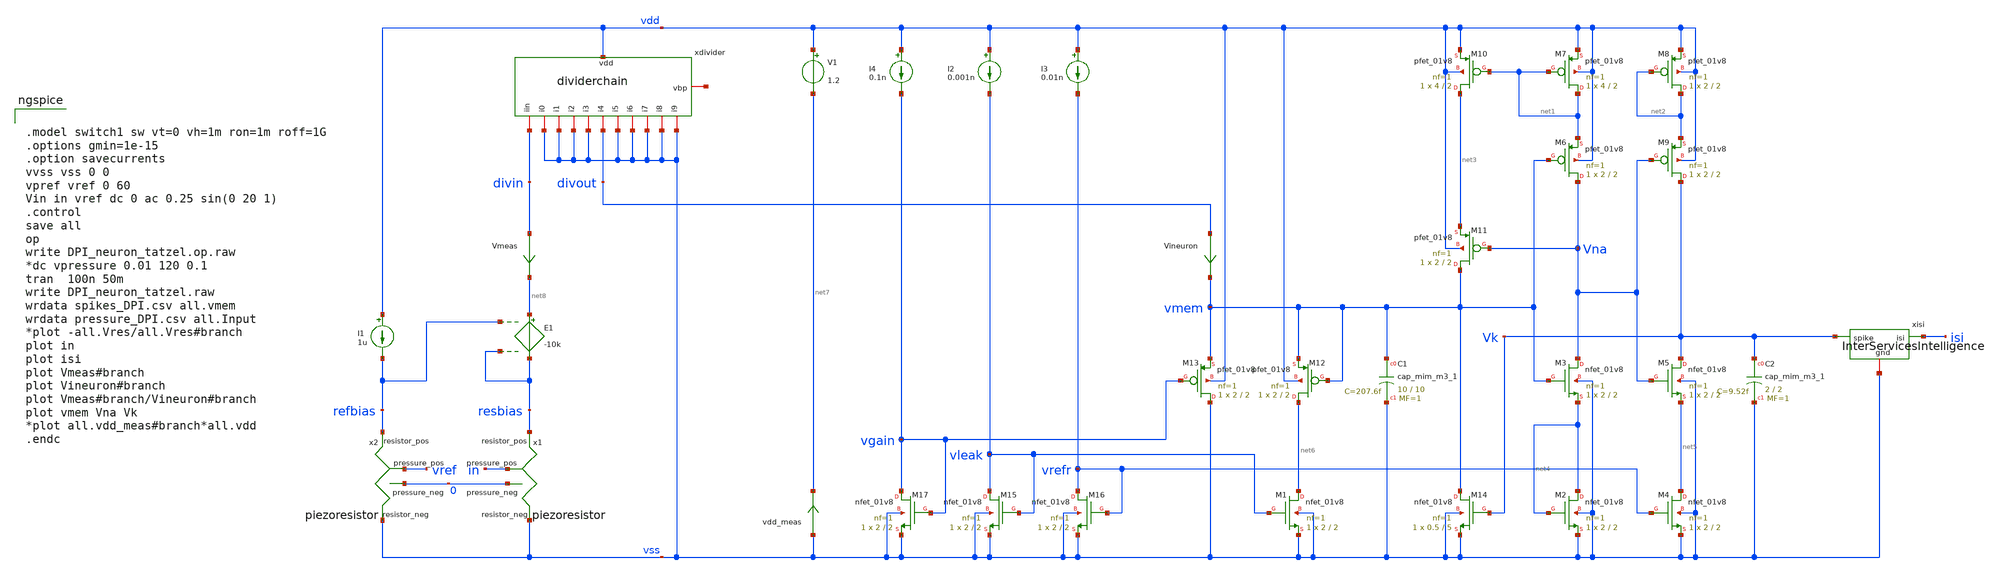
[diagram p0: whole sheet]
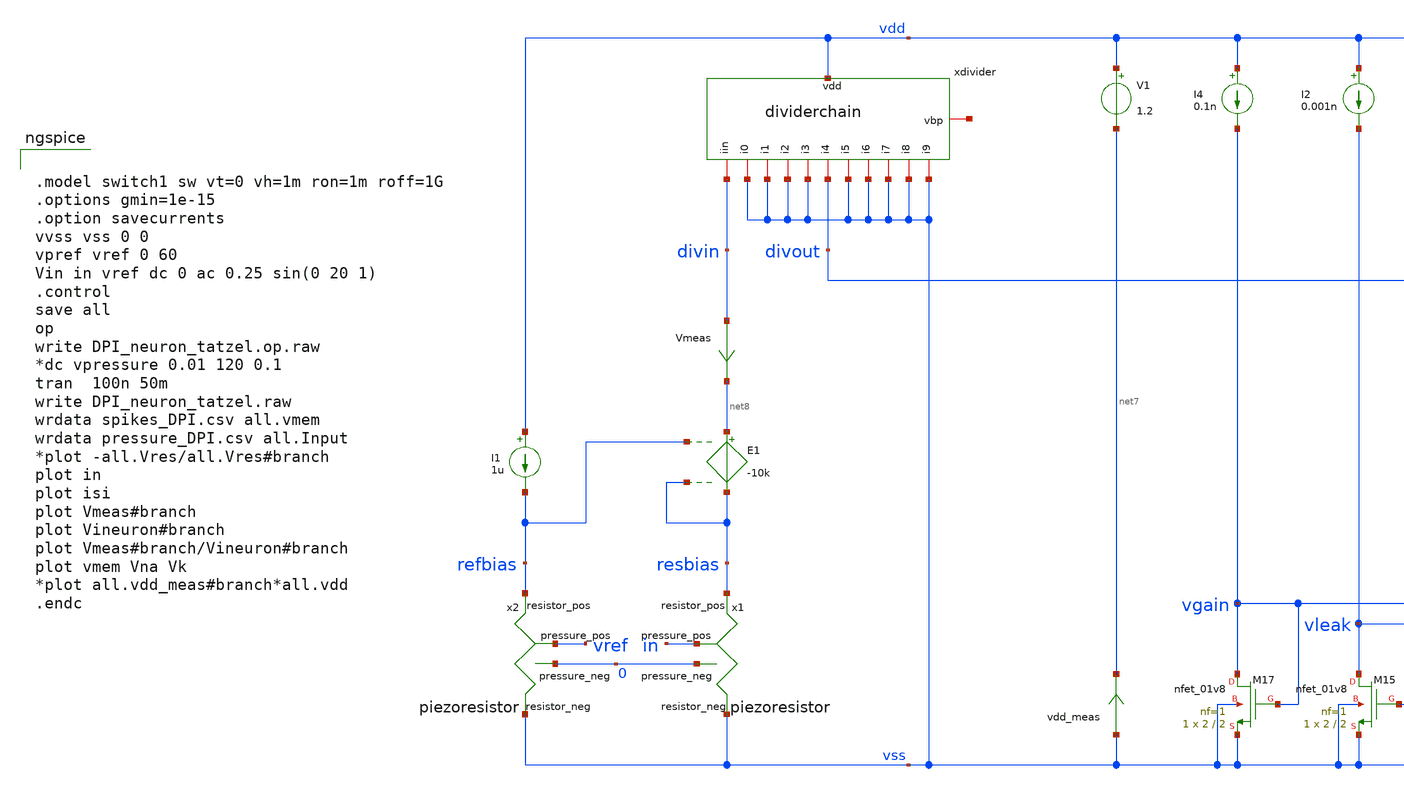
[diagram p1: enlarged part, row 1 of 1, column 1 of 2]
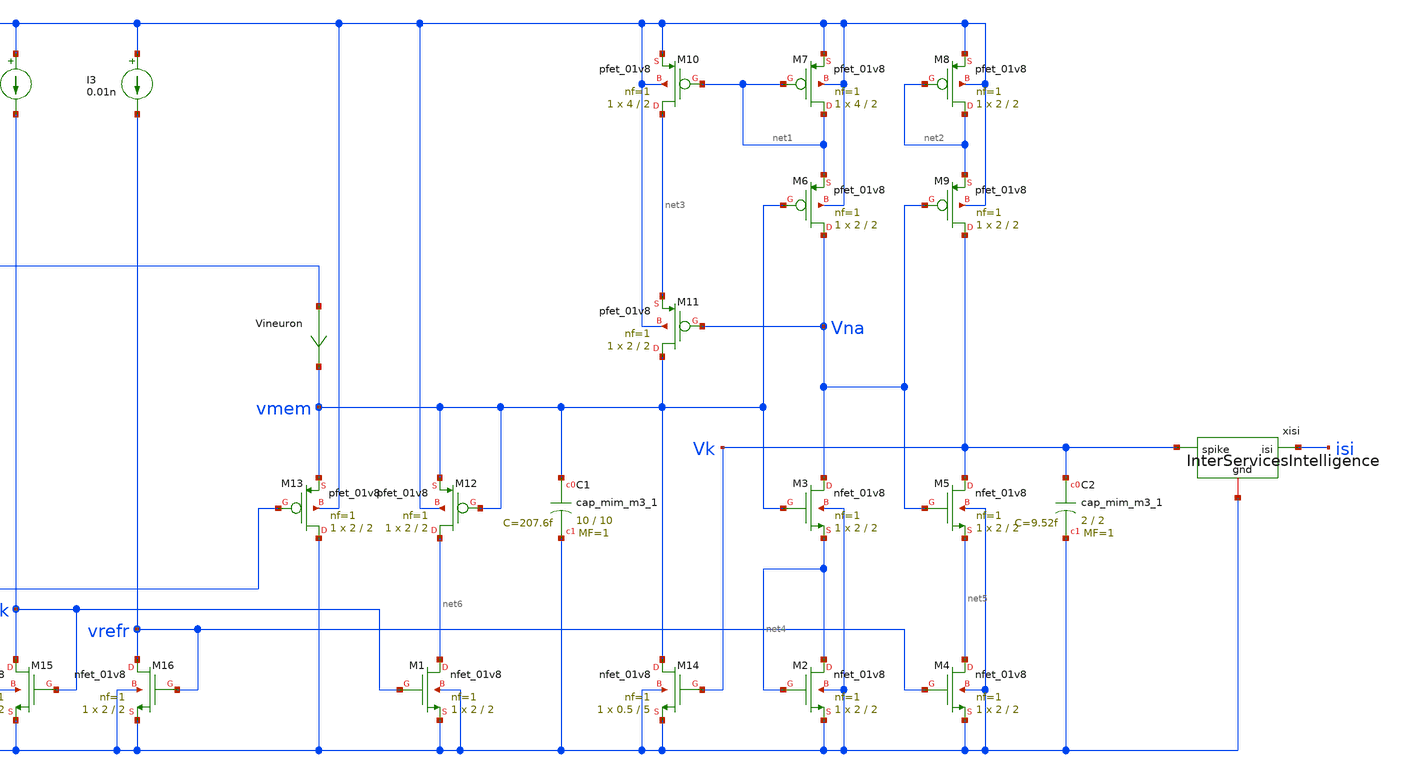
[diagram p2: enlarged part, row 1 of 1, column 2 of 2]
** sch_path: circuits/DPI_neuron_tatzel.sch
* piezoresistor.sch:
* Copyright 2020 Stefan Frederik Schippers
* Licensed under the Apache License, Version 2.0 (the "License");
**.subckt DPI_neuron_tatzel
Vmeas divin net8 0
.save i(vmeas)
vdd_meas vss net7 0
.save i(vdd_meas)
V1 vdd net7 1.2
XM1 net6 vleak vss vss sky130_fd_pr__nfet_01v8 L=2 W=2 nf=1 ad='int((nf+1)/2) * W/nf * 0.29' as='int((nf+2)/2) * W/nf * 0.29'
+ pd='2*int((nf+1)/2) * (W/nf + 0.29)' ps='2*int((nf+2)/2) * (W/nf + 0.29)' nrd='0.29 / W' nrs='0.29 / W'
+ sa=0 sb=0 sd=0 mult=1 m=1
XM2 net4 net4 vss vss sky130_fd_pr__nfet_01v8 L=2 W=2 nf=1 ad='int((nf+1)/2) * W/nf * 0.29' as='int((nf+2)/2) * W/nf * 0.29'
+ pd='2*int((nf+1)/2) * (W/nf + 0.29)' ps='2*int((nf+2)/2) * (W/nf + 0.29)' nrd='0.29 / W' nrs='0.29 / W'
+ sa=0 sb=0 sd=0 mult=1 m=1
XM3 Vna vmem net4 vss sky130_fd_pr__nfet_01v8 L=2 W=2 nf=1 ad='int((nf+1)/2) * W/nf * 0.29' as='int((nf+2)/2) * W/nf * 0.29'
+ pd='2*int((nf+1)/2) * (W/nf + 0.29)' ps='2*int((nf+2)/2) * (W/nf + 0.29)' nrd='0.29 / W' nrs='0.29 / W'
+ sa=0 sb=0 sd=0 mult=1 m=1
XC1 vmem vss sky130_fd_pr__cap_mim_m3_1 W=10 L=10 MF=1 m=1
XC2 Vk vss sky130_fd_pr__cap_mim_m3_1 W=2 L=2 MF=1 m=1
XM14 vmem Vk vss vss sky130_fd_pr__nfet_01v8 L=5 W=0.5 nf=1 ad='int((nf+1)/2) * W/nf * 0.29' as='int((nf+2)/2) * W/nf * 0.29'
+ pd='2*int((nf+1)/2) * (W/nf + 0.29)' ps='2*int((nf+2)/2) * (W/nf + 0.29)' nrd='0.29 / W' nrs='0.29 / W'
+ sa=0 sb=0 sd=0 mult=1 m=1
XM4 net5 vrefr vss vss sky130_fd_pr__nfet_01v8 L=2 W=2 nf=1 ad='int((nf+1)/2) * W/nf * 0.29' as='int((nf+2)/2) * W/nf * 0.29'
+ pd='2*int((nf+1)/2) * (W/nf + 0.29)' ps='2*int((nf+2)/2) * (W/nf + 0.29)' nrd='0.29 / W' nrs='0.29 / W'
+ sa=0 sb=0 sd=0 mult=1 m=1
XM5 Vk Vna net5 vss sky130_fd_pr__nfet_01v8 L=2 W=2 nf=1 ad='int((nf+1)/2) * W/nf * 0.29' as='int((nf+2)/2) * W/nf * 0.29'
+ pd='2*int((nf+1)/2) * (W/nf + 0.29)' ps='2*int((nf+2)/2) * (W/nf + 0.29)' nrd='0.29 / W' nrs='0.29 / W'
+ sa=0 sb=0 sd=0 mult=1 m=1
I2 vdd vleak 0.001n
XM15 vleak vleak vss vss sky130_fd_pr__nfet_01v8 L=2 W=2 nf=1 ad='int((nf+1)/2) * W/nf * 0.29' as='int((nf+2)/2) * W/nf * 0.29'
+ pd='2*int((nf+1)/2) * (W/nf + 0.29)' ps='2*int((nf+2)/2) * (W/nf + 0.29)' nrd='0.29 / W' nrs='0.29 / W'
+ sa=0 sb=0 sd=0 mult=1 m=1
I3 vdd vrefr 0.01n
XM16 vrefr vrefr vss vss sky130_fd_pr__nfet_01v8 L=2 W=2 nf=1 ad='int((nf+1)/2) * W/nf * 0.29' as='int((nf+2)/2) * W/nf * 0.29'
+ pd='2*int((nf+1)/2) * (W/nf + 0.29)' ps='2*int((nf+2)/2) * (W/nf + 0.29)' nrd='0.29 / W' nrs='0.29 / W'
+ sa=0 sb=0 sd=0 mult=1 m=1
I4 vdd vgain 0.1n
XM17 vgain vgain vss vss sky130_fd_pr__nfet_01v8 L=2 W=2 nf=1 ad='int((nf+1)/2) * W/nf * 0.29' as='int((nf+2)/2) * W/nf * 0.29'
+ pd='2*int((nf+1)/2) * (W/nf + 0.29)' ps='2*int((nf+2)/2) * (W/nf + 0.29)' nrd='0.29 / W' nrs='0.29 / W'
+ sa=0 sb=0 sd=0 mult=1 m=1
XM6 Vna vmem net1 vdd sky130_fd_pr__pfet_01v8 L=2 W=2 nf=1 ad='int((nf+1)/2) * W/nf * 0.29' as='int((nf+2)/2) * W/nf * 0.29'
+ pd='2*int((nf+1)/2) * (W/nf + 0.29)' ps='2*int((nf+2)/2) * (W/nf + 0.29)' nrd='0.29 / W' nrs='0.29 / W'
+ sa=0 sb=0 sd=0 mult=1 m=1
XM7 net1 net1 vdd vdd sky130_fd_pr__pfet_01v8 L=2 W=4 nf=1 ad='int((nf+1)/2) * W/nf * 0.29' as='int((nf+2)/2) * W/nf * 0.29'
+ pd='2*int((nf+1)/2) * (W/nf + 0.29)' ps='2*int((nf+2)/2) * (W/nf + 0.29)' nrd='0.29 / W' nrs='0.29 / W'
+ sa=0 sb=0 sd=0 mult=1 m=1
XM8 net2 net2 vdd vdd sky130_fd_pr__pfet_01v8 L=2 W=2 nf=1 ad='int((nf+1)/2) * W/nf * 0.29' as='int((nf+2)/2) * W/nf * 0.29'
+ pd='2*int((nf+1)/2) * (W/nf + 0.29)' ps='2*int((nf+2)/2) * (W/nf + 0.29)' nrd='0.29 / W' nrs='0.29 / W'
+ sa=0 sb=0 sd=0 mult=1 m=1
XM9 Vk Vna net2 vdd sky130_fd_pr__pfet_01v8 L=2 W=2 nf=1 ad='int((nf+1)/2) * W/nf * 0.29' as='int((nf+2)/2) * W/nf * 0.29'
+ pd='2*int((nf+1)/2) * (W/nf + 0.29)' ps='2*int((nf+2)/2) * (W/nf + 0.29)' nrd='0.29 / W' nrs='0.29 / W'
+ sa=0 sb=0 sd=0 mult=1 m=1
XM10 net3 net1 vdd vdd sky130_fd_pr__pfet_01v8 L=2 W=4 nf=1 ad='int((nf+1)/2) * W/nf * 0.29' as='int((nf+2)/2) * W/nf * 0.29'
+ pd='2*int((nf+1)/2) * (W/nf + 0.29)' ps='2*int((nf+2)/2) * (W/nf + 0.29)' nrd='0.29 / W' nrs='0.29 / W'
+ sa=0 sb=0 sd=0 mult=1 m=1
XM11 vmem Vna net3 vdd sky130_fd_pr__pfet_01v8 L=2 W=2 nf=1 ad='int((nf+1)/2) * W/nf * 0.29' as='int((nf+2)/2) * W/nf * 0.29'
+ pd='2*int((nf+1)/2) * (W/nf + 0.29)' ps='2*int((nf+2)/2) * (W/nf + 0.29)' nrd='0.29 / W' nrs='0.29 / W'
+ sa=0 sb=0 sd=0 mult=1 m=1
XM12 net6 vmem vmem vdd sky130_fd_pr__pfet_01v8 L=2 W=2 nf=1 ad='int((nf+1)/2) * W/nf * 0.29' as='int((nf+2)/2) * W/nf * 0.29'
+ pd='2*int((nf+1)/2) * (W/nf + 0.29)' ps='2*int((nf+2)/2) * (W/nf + 0.29)' nrd='0.29 / W' nrs='0.29 / W'
+ sa=0 sb=0 sd=0 mult=1 m=1
XM13 vss vgain vmem vdd sky130_fd_pr__pfet_01v8 L=2 W=2 nf=1 ad='int((nf+1)/2) * W/nf * 0.29' as='int((nf+2)/2) * W/nf * 0.29'
+ pd='2*int((nf+1)/2) * (W/nf + 0.29)' ps='2*int((nf+2)/2) * (W/nf + 0.29)' nrd='0.29 / W' nrs='0.29 / W'
+ sa=0 sb=0 sd=0 mult=1 m=1
x1 in 0 resbias vss piezoresistor
x2 vref 0 refbias vss piezoresistor
xdivider vdd net9 divin vss vss vss vss divout vss vss vss vss vss dividerchain
Vineuron divout vmem 0
.save i(vineuron)
I1 vdd refbias 1u
E1 net8 resbias refbias resbias -10k
xisi isi Vk vss InterServicesIntelligence
**** begin user architecture code


.model switch1 sw vt=0 vh=1m ron=1m roff=1G
.options gmin=1e-15
.option savecurrents
vvss vss 0 0
vpref vref 0 60
Vin in vref dc 0 ac 0.25 sin(0 20 1)
.control
save all
op
write DPI_neuron_tatzel.op.raw
*dc vpressure 0.01 120 0.1
tran  100n 50m
write DPI_neuron_tatzel.raw
wrdata spikes_DPI.csv all.vmem
wrdata pressure_DPI.csv all.Input
*plot -all.Vres/all.Vres#branch
plot in
plot isi
plot Vmeas#branch
plot Vineuron#branch
plot Vmeas#branch/Vineuron#branch
plot vmem Vna Vk
*plot all.vdd_meas#branch*all.vdd
.endc


 .lib $::SKYWATER_MODELS/models/sky130.lib.spice tt

.param mc_mm_switch=0
.param mc_pr_switch=1


**** end user architecture code
**.ends

* expanding   symbol:  /home/cmaier/.xschem/sky130_TAC3/circuits/piezoresistor.sym # of pins=4
** sym_path: circuits/piezoresistor.sym
** sch_path: circuits/piezoresistor.sch
.subckt piezoresistor pressure_pos pressure_neg resistor_pos resistor_neg
*.ipin pressure_pos
*.ipin pressure_neg
*.iopin resistor_pos
*.iopin resistor_neg
Broot sqrtp 0 V = sqrt(v(pressure_pos,pressure_neg))
Bres res 0 V = 106*(50/v(sqrtp)-1)*exp(-0.328*v(sqrtp))+15
Brvar resistor_pos resistor_neg I = V(resistor_pos,resistor_neg)/V(res)
.ends


* expanding   symbol:  ../playground/dividerchain.sym # of pins=13
** sym_path: playground/dividerchain.sym
** sch_path: playground/dividerchain.sch
.subckt dividerchain vdd vbp iin i0 i1 i2 i3 i4 i5 i6 i7 i8 i9
*.iopin vdd
*.iopin iin
*.iopin vbp
*.iopin i0
*.iopin i1
*.iopin i2
*.iopin i3
*.iopin i4
*.iopin i5
*.iopin i6
*.iopin i7
*.iopin i8
*.iopin i9
Viin vbp iin 0
.save i(viin)
Vi0 net18 i0 0
.save i(vi0)
Vi01 vdd net1 0
.save i(vi01)
Vi1 net2 i1 0
.save i(vi1)
Vi12 net3 net4 0
.save i(vi12)
Vi2 net5 i2 0
.save i(vi2)
Vi23 net19 net6 0
.save i(vi23)
Vi3 net7 i3 0
.save i(vi3)
Vi34 net20 net8 0
.save i(vi34)
Vi4 net9 i4 0
.save i(vi4)
Vi45 net21 net10 0
.save i(vi45)
Vi5 net11 i5 0
.save i(vi5)
Vi56 net22 net12 0
.save i(vi56)
Vi6 net13 i6 0
.save i(vi6)
Vi67 net23 net14 0
.save i(vi67)
Vi7 net15 i7 0
.save i(vi7)
Vi78 net24 net16 0
.save i(vi78)
Vi8 net17 i8 0
.save i(vi8)
Vi9 net26 i9 0
.save i(vi9)
x1 vdd net1 net3 vbp net2 divider
x2 vdd net4 net19 vbp net5 divider
x3 vdd net6 net20 vbp net7 divider
x4 vdd net8 net21 vbp net9 divider
x5 vdd net10 net22 vbp net11 divider
x6 vdd net12 net23 vbp net13 divider
x7 vdd net14 net24 vbp net15 divider
x8 vdd net16 net25 vbp net17 divider
XM1 vbp vbp vdd vdd sky130_fd_pr__pfet_01v8 L=2 W=1 nf=1 ad='int((nf+1)/2) * W/nf * 0.29' as='int((nf+2)/2) * W/nf * 0.29'
+ pd='2*int((nf+1)/2) * (W/nf + 0.29)' ps='2*int((nf+2)/2) * (W/nf + 0.29)' nrd='0.29 / W' nrs='0.29 / W'
+ sa=0 sb=0 sd=0 mult=1 m=1
XM2 net18 vbp vdd vdd sky130_fd_pr__pfet_01v8 L=2 W=1 nf=1 ad='int((nf+1)/2) * W/nf * 0.29' as='int((nf+2)/2) * W/nf * 0.29'
+ pd='2*int((nf+1)/2) * (W/nf + 0.29)' ps='2*int((nf+2)/2) * (W/nf + 0.29)' nrd='0.29 / W' nrs='0.29 / W'
+ sa=0 sb=0 sd=0 mult=1 m=1
XM3 net26 vbp net25 vdd sky130_fd_pr__pfet_01v8 L=32 W=1 nf=1 ad='int((nf+1)/2) * W/nf * 0.29' as='int((nf+2)/2) * W/nf * 0.29'
+ pd='2*int((nf+1)/2) * (W/nf + 0.29)' ps='2*int((nf+2)/2) * (W/nf + 0.29)' nrd='0.29 / W' nrs='0.29 / W'
+ sa=0 sb=0 sd=0 mult=1 m=1
.ends


* expanding   symbol:  /home/cmaier/.xschem/sky130_TAC3/playground/InterServicesIntelligence.sym #
*+ of pins=3
** sym_path: playground/InterServicesIntelligence.sym
** sch_path: playground/InterServicesIntelligence.sch
.subckt InterServicesIntelligence isi spike gnd
*.iopin gnd
*.ipin spike
*.opin isi
Csample sample gnd 100f m=1
Itiming gnd sample 1n
Sreset sample gnd dspikedt net1 SWITCH1
Cintegrate isi gnd 10f m=1
Vreset net1 gnd 200m
Soff sample isi voff dspikedt SWITCH1
Vsample voff gnd -200m
Ebuffer spikebuf gnd spike gnd 1
Cdiff net2 gnd 1u m=1
Vmeas spikebuf net2 0
.save i(vmeas)
Hdiff dspikedt gnd vmeas 1
.ends


* expanding   symbol:  divider.sym # of pins=5
** sym_path: playground/divider.sym
** sch_path: playground/divider.sch
.subckt divider vdd iin iout vbp isink
*.iopin iin
*.iopin vdd
*.iopin vbp
*.iopin iout
*.iopin isink
XM12 node vbp net1 vdd sky130_fd_pr__pfet_01v8 L=31 W=1 nf=1 ad='int((nf+1)/2) * W/nf * 0.29' as='int((nf+2)/2) * W/nf * 0.29'
+ pd='2*int((nf+1)/2) * (W/nf + 0.29)' ps='2*int((nf+2)/2) * (W/nf + 0.29)' nrd='0.29 / W' nrs='0.29 / W'
+ sa=0 sb=0 sd=0 mult=1 m=1
Viin iin net1 0
.save i(viin)
Viout node iout 0
.save i(viout)
XM1 net2 vbp node vdd sky130_fd_pr__pfet_01v8 L=2 W=1 nf=1 ad='int((nf+1)/2) * W/nf * 0.29' as='int((nf+2)/2) * W/nf * 0.29'
+ pd='2*int((nf+1)/2) * (W/nf + 0.29)' ps='2*int((nf+2)/2) * (W/nf + 0.29)' nrd='0.29 / W' nrs='0.29 / W'
+ sa=0 sb=0 sd=0 mult=1 m=1
Visink net2 isink 0
.save i(visink)
.ends

.end
